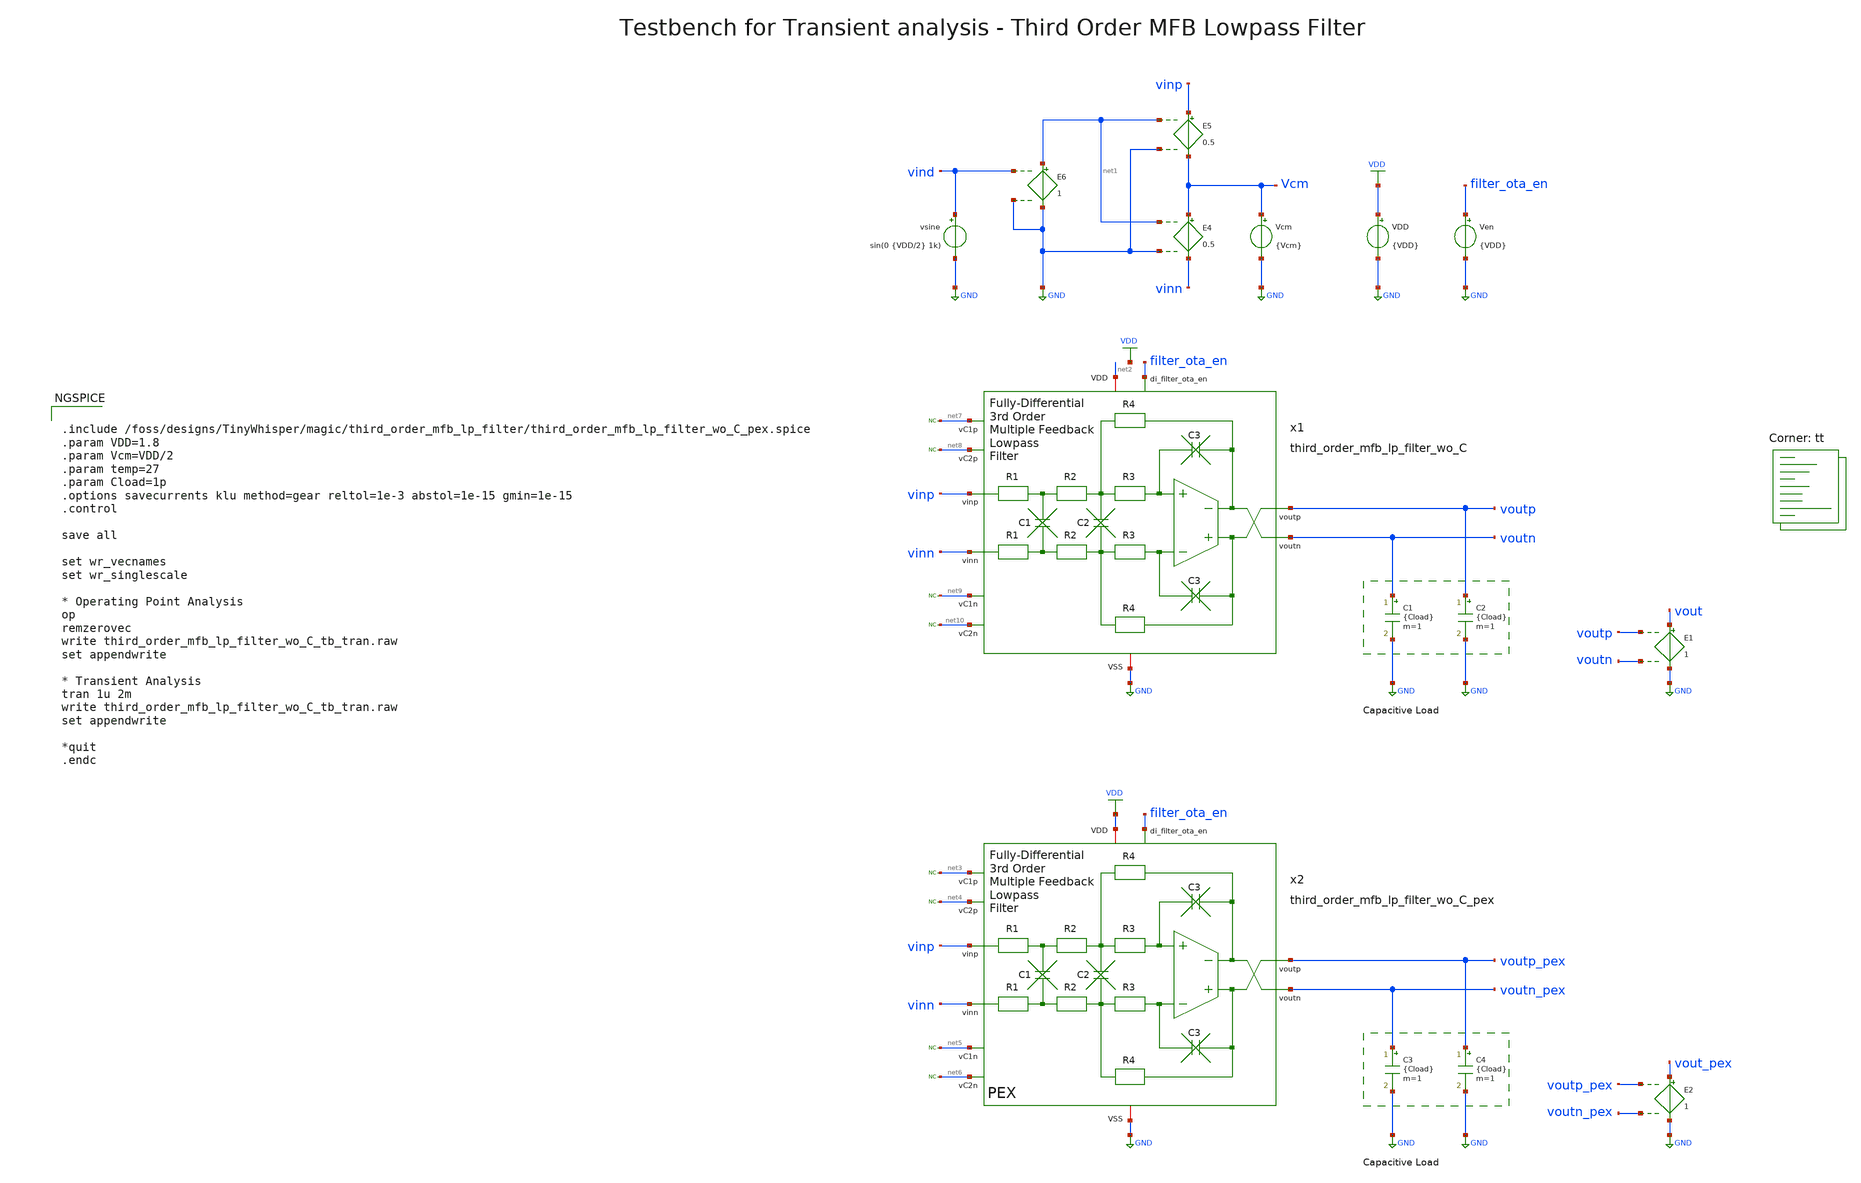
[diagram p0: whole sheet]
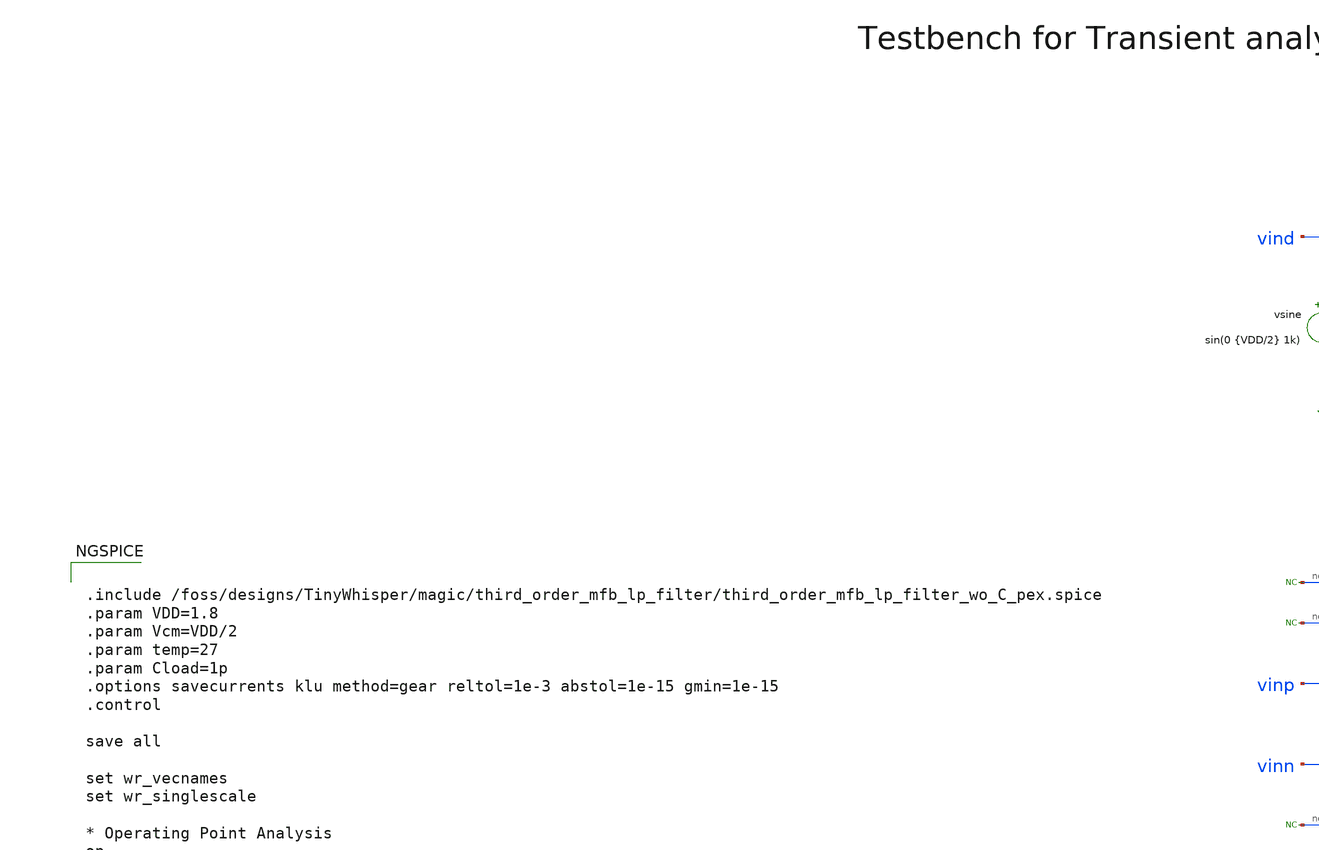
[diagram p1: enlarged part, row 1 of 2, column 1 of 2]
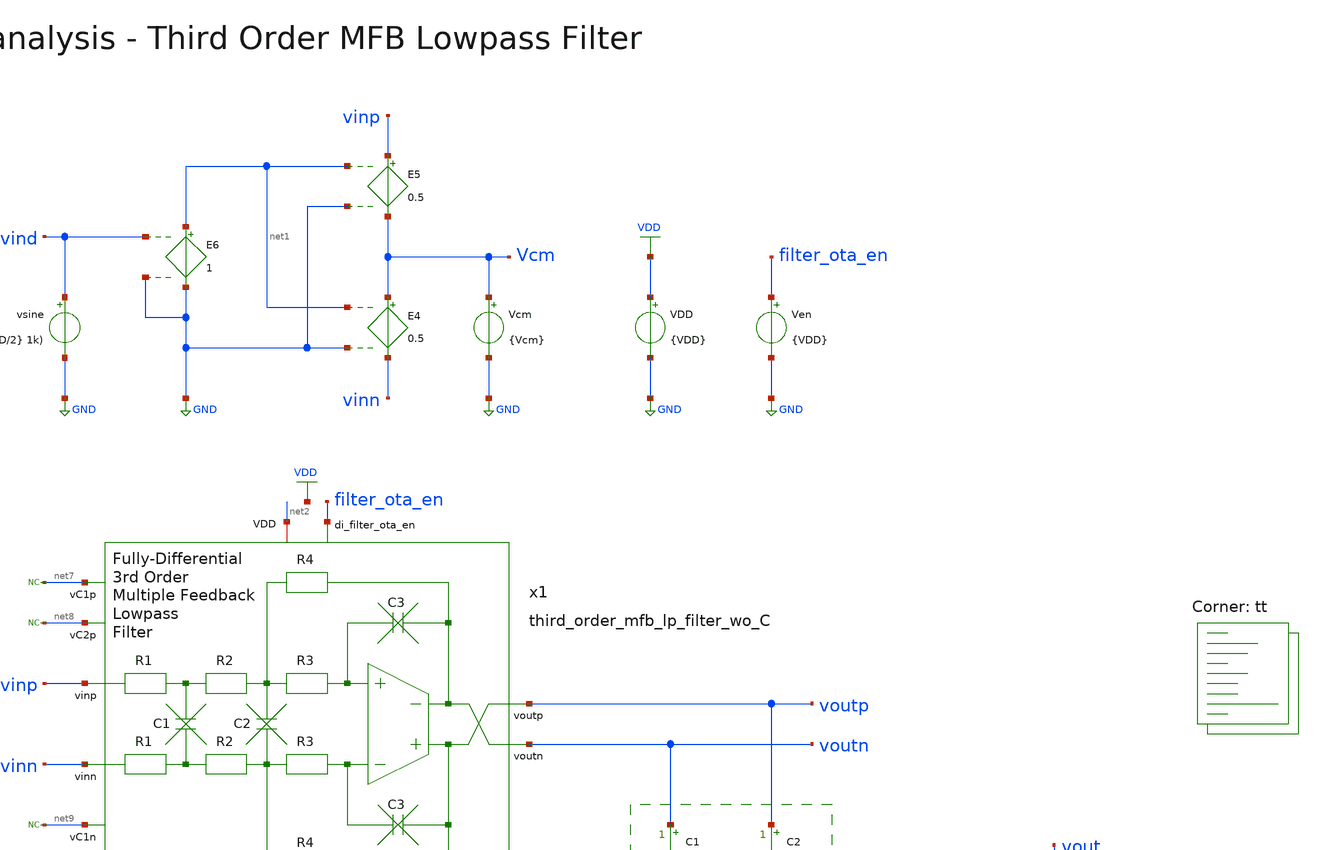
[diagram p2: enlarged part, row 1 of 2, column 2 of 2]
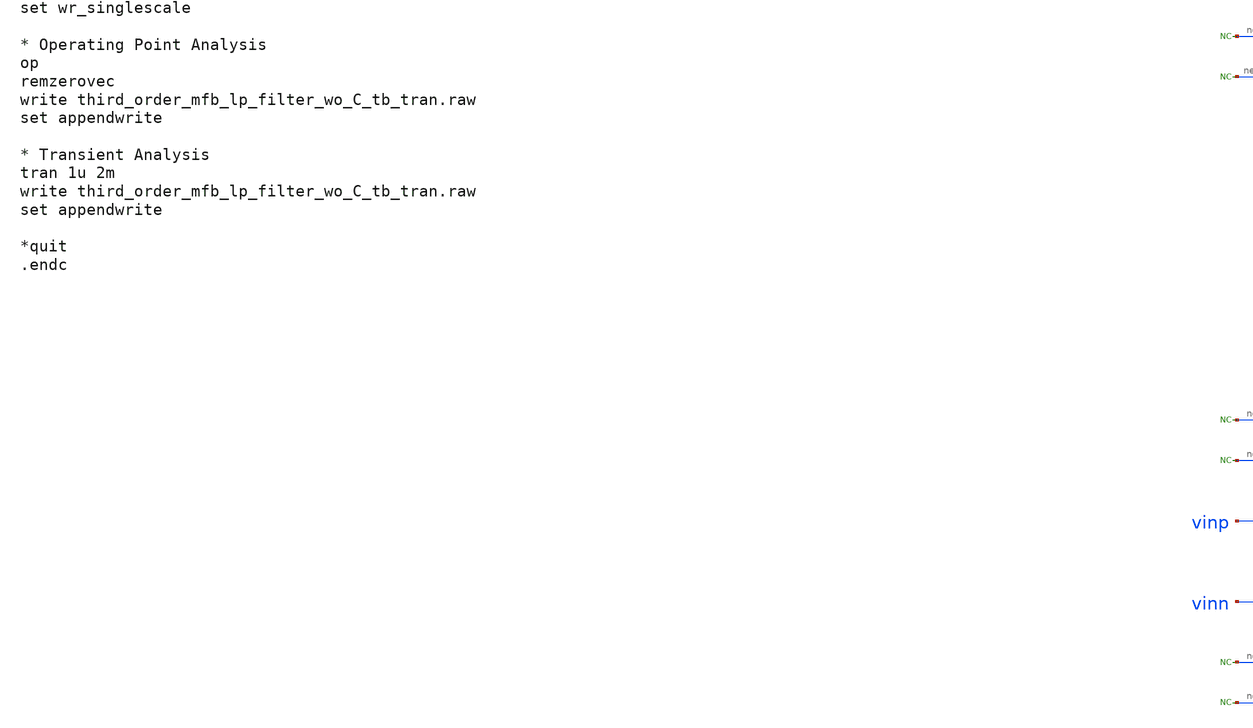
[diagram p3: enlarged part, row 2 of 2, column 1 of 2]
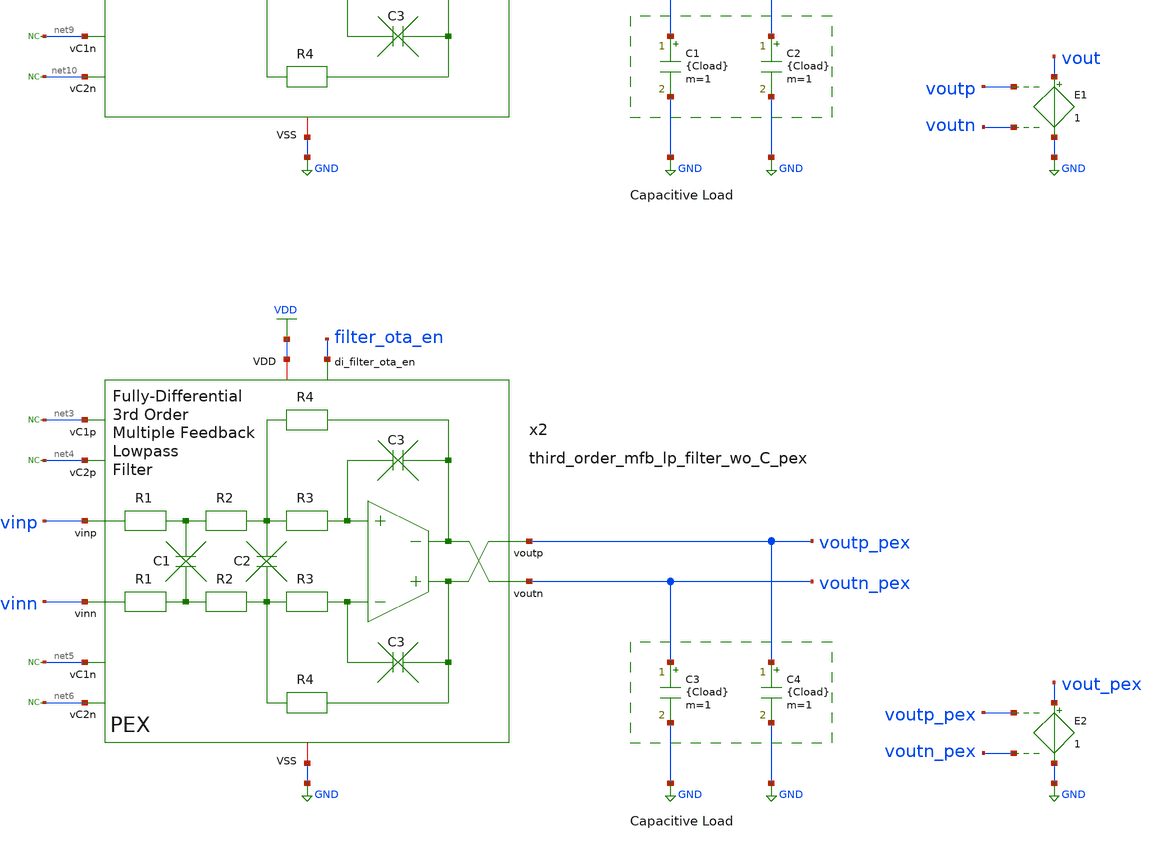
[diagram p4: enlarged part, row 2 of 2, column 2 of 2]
** sch_path: magic/iq_modulator/third_order_mfb_lp_filter/third_order_mfb_lp_filter_wo_C_tb_tran.sch
**.subckt third_order_mfb_lp_filter_wo_C_tb_tran
VDD VDD GND {VDD}
C1 voutn GND {Cload} m=1
C2 voutp GND {Cload} m=1
Vcm Vcm GND {Vcm}
E4 Vcm vinn net1 GND 0.5
E5 vinp Vcm net1 GND 0.5
E6 net1 GND vind GND 1
Ven filter_ota_en GND {VDD}
E1 vout GND voutp voutn 1
x1 filter_ota_en voutp vinp voutn vinn net2 GND net8 net7 net10 net9 third_order_mfb_lp_filter_wo_C
C3 voutn_pex GND {Cload} m=1
C4 voutp_pex GND {Cload} m=1
E2 vout_pex GND voutp_pex voutn_pex 1
* noconn #net7
* noconn #net8
* noconn #net9
* noconn #net10
* noconn #net3
* noconn #net4
* noconn #net5
* noconn #net6
vsine vind GND sin(0 {VDD/2} 1k)
x2 vinp vinn net3 net5 net6 net4 filter_ota_en voutn_pex voutp_pex VDD GND
+ third_order_mfb_lp_filter_wo_C_pex
**** begin user architecture code


.include /foss/designs/TinyWhisper/magic/third_order_mfb_lp_filter/third_order_mfb_lp_filter_wo_C_pex.spice
.param VDD=1.8
.param Vcm=VDD/2
.param temp=27
.param Cload=1p
.options savecurrents klu method=gear reltol=1e-3 abstol=1e-15 gmin=1e-15
.control

save all

set wr_vecnames
set wr_singlescale

* Operating Point Analysis
op
remzerovec
write third_order_mfb_lp_filter_wo_C_tb_tran.raw
set appendwrite

* Transient Analysis
tran 1u 2m
write third_order_mfb_lp_filter_wo_C_tb_tran.raw
set appendwrite

*quit
.endc


.lib $::SKYWATER_MODELS/sky130.lib.spice tt
**** end user architecture code
**.ends
.GLOBAL GND
.GLOBAL VDD
.end
